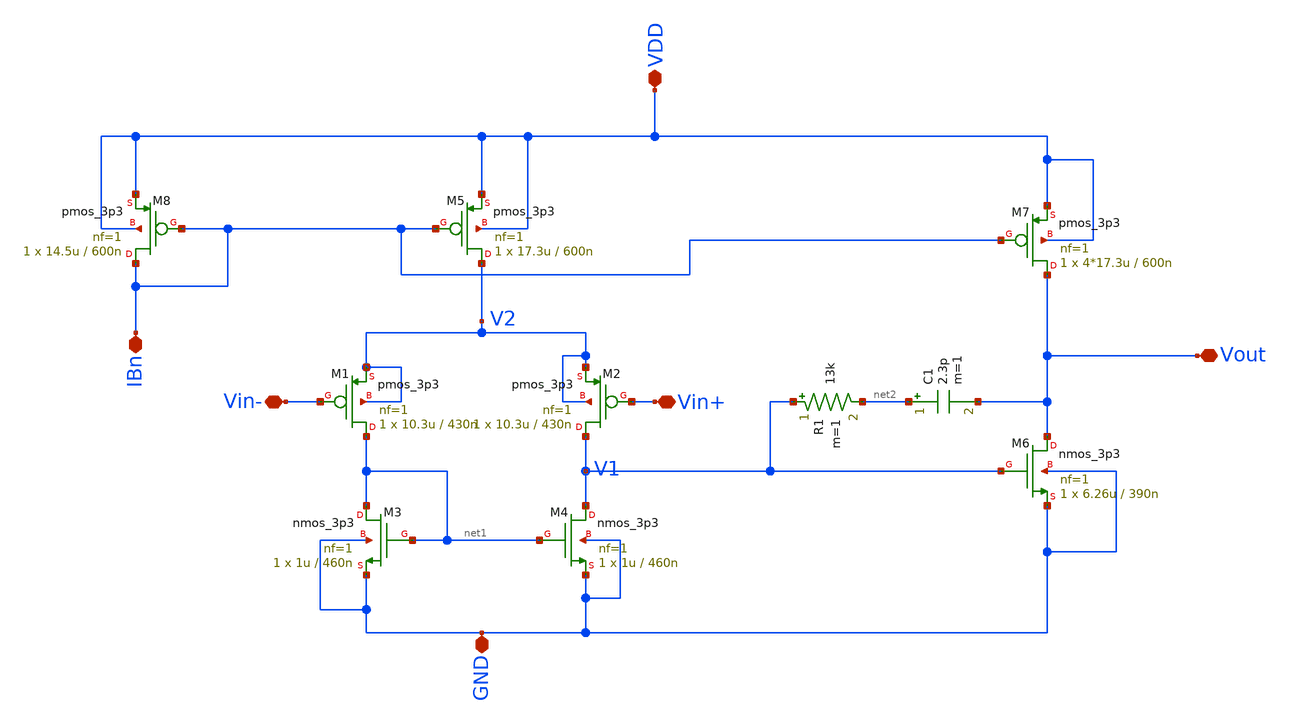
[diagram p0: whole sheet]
** sch_path: ITI_Labs/Lab9_Xschem/Design/Lab09.sch
**.subckt Lab09 VDD GND IBn Vin- Vin+ Vout
*.iopin VDD
*.iopin GND
*.iopin IBn
*.iopin Vin-
*.iopin Vin+
*.iopin Vout
XM2 V1 Vin+ V2 V2 pmos_3p3 L=430n W=10.3u nf=1 ad='int((nf+1)/2) * W/nf * 0.18u' as='int((nf+2)/2) * W/nf * 0.18u'
+ pd='2*int((nf+1)/2) * (W/nf + 0.18u)' ps='2*int((nf+2)/2) * (W/nf + 0.18u)' nrd='0.18u / W' nrs='0.18u / W'
+ sa=0 sb=0 sd=0 m=1
XM3 net1 net1 GND GND nmos_3p3 L=460n W=1u nf=1 ad='int((nf+1)/2) * W/nf * 0.18u' as='int((nf+2)/2) * W/nf * 0.18u'
+ pd='2*int((nf+1)/2) * (W/nf + 0.18u)' ps='2*int((nf+2)/2) * (W/nf + 0.18u)' nrd='0.18u / W' nrs='0.18u / W'
+ sa=0 sb=0 sd=0 m=1
XM4 V1 net1 GND GND nmos_3p3 L=460n W=1u nf=1 ad='int((nf+1)/2) * W/nf * 0.18u' as='int((nf+2)/2) * W/nf * 0.18u'
+ pd='2*int((nf+1)/2) * (W/nf + 0.18u)' ps='2*int((nf+2)/2) * (W/nf + 0.18u)' nrd='0.18u / W' nrs='0.18u / W'
+ sa=0 sb=0 sd=0 m=1
XM1 net1 Vin- V2 V2 pmos_3p3 L=430n W=10.3u nf=1 ad='int((nf+1)/2) * W/nf * 0.18u' as='int((nf+2)/2) * W/nf * 0.18u'
+ pd='2*int((nf+1)/2) * (W/nf + 0.18u)' ps='2*int((nf+2)/2) * (W/nf + 0.18u)' nrd='0.18u / W' nrs='0.18u / W'
+ sa=0 sb=0 sd=0 m=1
XM5 V2 IBn VDD VDD pmos_3p3 L=600n W=17.3u nf=1 ad='int((nf+1)/2) * W/nf * 0.18u' as='int((nf+2)/2) * W/nf * 0.18u'
+ pd='2*int((nf+1)/2) * (W/nf + 0.18u)' ps='2*int((nf+2)/2) * (W/nf + 0.18u)' nrd='0.18u / W' nrs='0.18u / W'
+ sa=0 sb=0 sd=0 m=1
XM6 Vout V1 GND GND nmos_3p3 L=390n W=6.26u nf=1 ad='int((nf+1)/2) * W/nf * 0.18u' as='int((nf+2)/2) * W/nf * 0.18u'
+ pd='2*int((nf+1)/2) * (W/nf + 0.18u)' ps='2*int((nf+2)/2) * (W/nf + 0.18u)' nrd='0.18u / W' nrs='0.18u / W'
+ sa=0 sb=0 sd=0 m=1
XM8 IBn IBn VDD VDD pmos_3p3 L=600n W=14.5u nf=1 ad='int((nf+1)/2) * W/nf * 0.18u' as='int((nf+2)/2) * W/nf * 0.18u'
+ pd='2*int((nf+1)/2) * (W/nf + 0.18u)' ps='2*int((nf+2)/2) * (W/nf + 0.18u)' nrd='0.18u / W' nrs='0.18u / W'
+ sa=0 sb=0 sd=0 m=1
R1 V1 net2 13k m=1
C1 net2 Vout 2.3p m=1
XM7 Vout IBn VDD VDD pmos_3p3 L=600n W=4*17.3u nf=1 ad='int((nf+1)/2) * W/nf * 0.18u' as='int((nf+2)/2) * W/nf * 0.18u'
+ pd='2*int((nf+1)/2) * (W/nf + 0.18u)' ps='2*int((nf+2)/2) * (W/nf + 0.18u)' nrd='0.18u / W' nrs='0.18u / W'
+ sa=0 sb=0 sd=0 m=1
**.ends
.end
